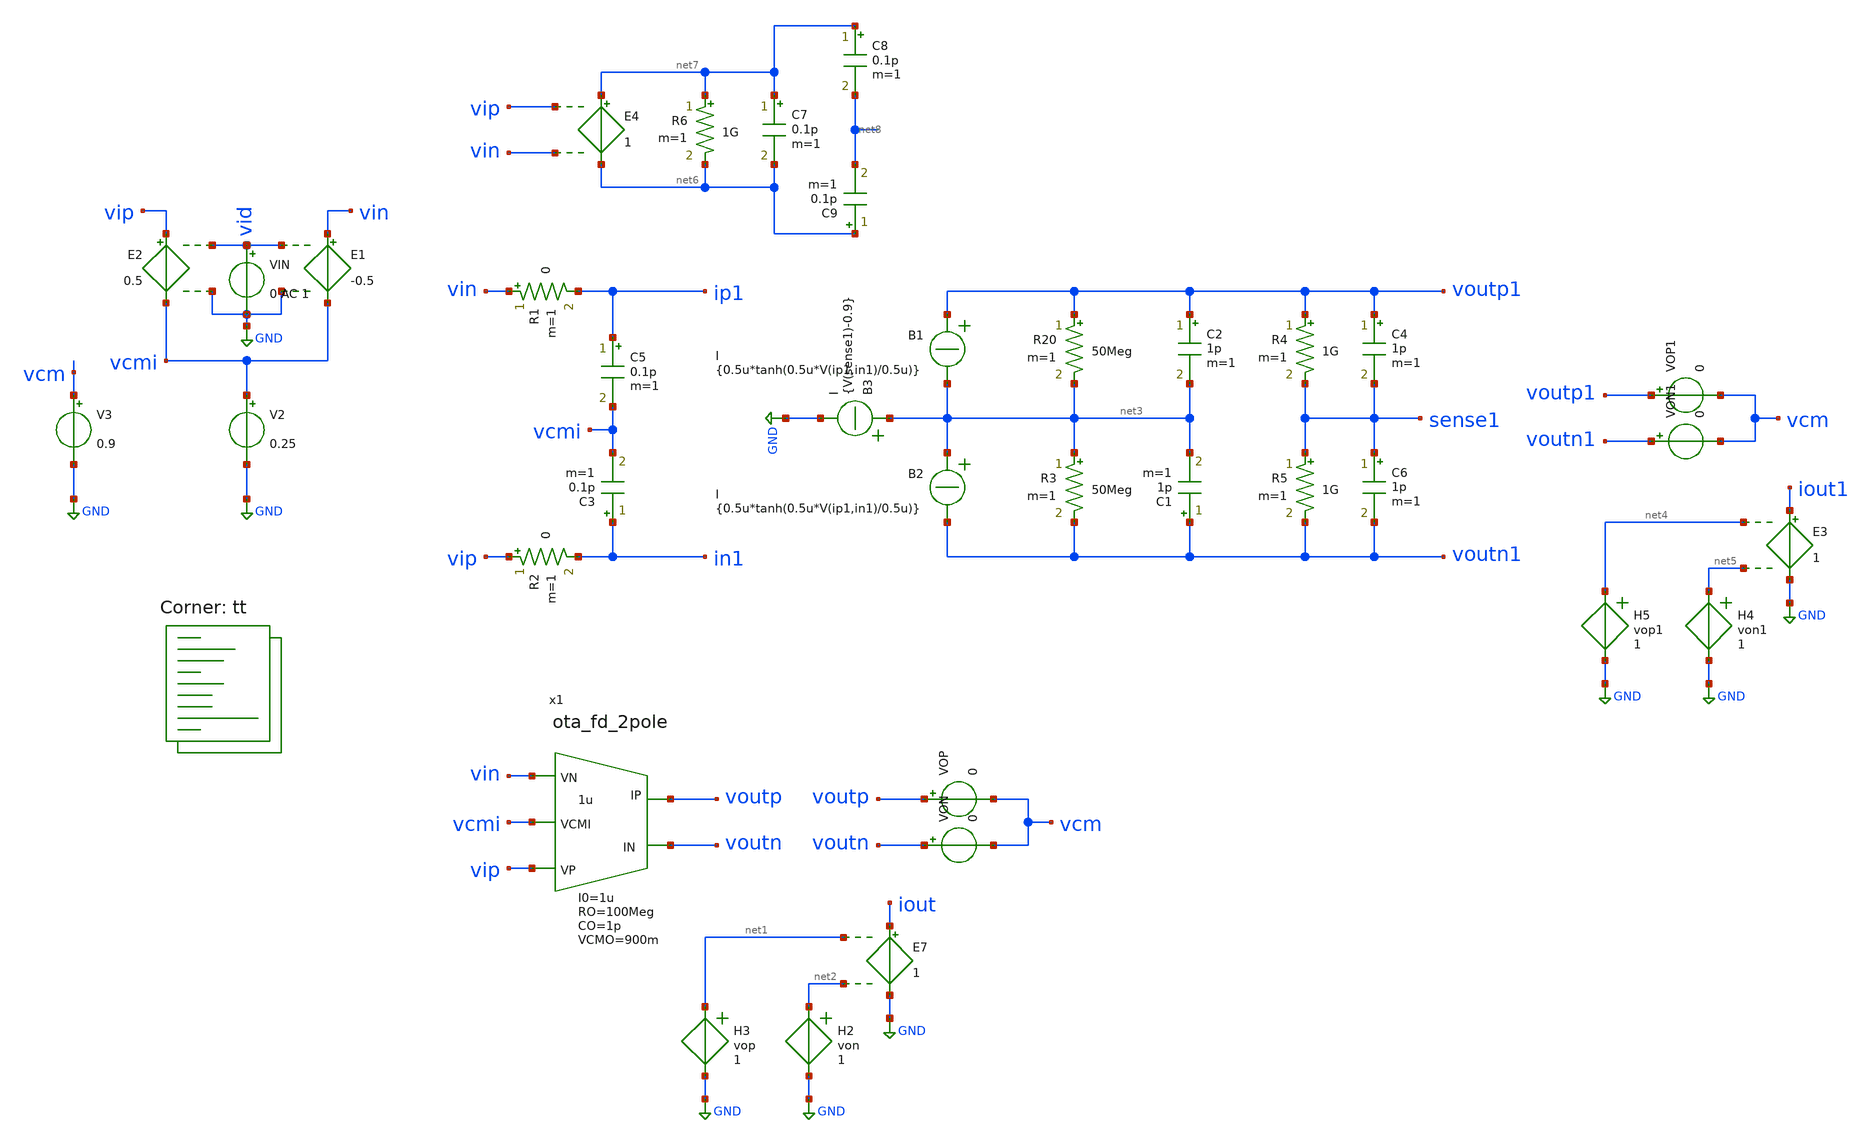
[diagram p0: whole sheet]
** sch_path: circuit-level/xschem/macro-models/ota_macro_fullydiff.sch
**.subckt ota_macro_fullydiff
V2 vcmi GND 0.25
E1 vin vcmi vid GND -0.5
E2 vip vcmi vid GND 0.5
VIN vid GND 0 AC 1
E7 iout GND net1 net2 1
R20 voutp1 net3 50Meg m=1
R3 net3 voutn1 50Meg m=1
C5 ip1 vcmi 0.1p m=1
C3 in1 vcmi 0.1p m=1
V3 vcm GND 0.9
R1 vin ip1 0 m=1
R2 vip in1 0 m=1
C1 voutn1 net3 1p m=1
C2 voutp1 net3 1p m=1
B1 voutp1 net3 I = {0.5u*tanh(0.5u*V(ip1,in1)/0.5u)}
B2 net3 voutn1 I = {0.5u*tanh(0.5u*V(ip1,in1)/0.5u)}
R4 voutp1 sense1 1G m=1
R5 sense1 voutn1 1G m=1
VOP voutp vcm 0
VON voutn vcm 0
H2 net2 GND von 1
H3 net1 GND vop 1
VOP1 voutp1 vcm 0
VON1 voutn1 vcm 0
E3 iout1 GND net4 net5 1
H4 net5 GND von1 1
H5 net4 GND vop1 1
C4 voutp1 sense1 1p m=1
C6 sense1 voutn1 1p m=1
B3 net3 GND I = {V(sense1)-0.9}
x1 vin voutp voutn vip vcmi ota_fd_2pole GM=1u RO=100Meg CO=1p RP=0 CP=0.1p VCMO=900m I0=1u
E4 net7 net6 vip vin 1
C7 net7 net6 0.1p m=1
R6 net7 net6 1G m=1
C8 net7 net8 0.1p m=1
C9 net6 net8 0.1p m=1
**** begin user architecture code
.lib $::SKYWATER_MODELS/sky130.lib.spice tt


.options savecurrents
.control
save all

let f_sig = 18
let tper_sig = 1/f_sig
let tfr_sig = tper_sig/2
*alter @VIN[PULSE]=[ -0.8 0.8 0 $&tfr_sig $&tfr_sig 1u $&tper_sig 0 ]
alter @VIN[SIN] = [ 0 0.1 $&f_sig 0 0 0 ]
alter @VIN[DC] = 0.0

let tstep = 0.01/f_sig
let tstop = 100/f_sig
let tstart = 0

** Main Simulations
let rl = 1Meg
let pltnr = 1
.options scale = 1
while const.pltnr le 1

	dc VIN -0.81 0.81 0.008

	ac dec 1000 0.1 1e9

	tran $&tstep $&tstop $&tstart


	set pltName = ac$&const.pltnr
       	setplot $pltName
	*setplot ac1
	let A_cell = v(iout)/v(vid)
	plot vdb(A_cell) 180/PI*cph(A_cell)
	let A1 = v(iout1)/v(vid)
	plot vdb(A1) 180/PI*cph(A1)

	set pltName = dc$&const.pltnr
       	setplot $pltName
	*setplot dc1
	let vid = v(vid)


	*let iop = v1#branch
	*let ion = v3#branch
	*let iod = iop-ion

	*plot iod ion iop

	setplot tran1
	let vcmo_cell = (voutp+voutn)/2
	let vcmo_1 = (voutp1+voutn1)/2
	let iop_cell = vop#branch
	let ion_cell = von#branch
	let iop_1 = vop1#branch
	let ion_1 = von1#branch
	let io_diff_cell = vop#branch - von#branch
	let io_diff_1 = vop1#branch - von1#branch
	let gm_cell = abs(io_diff_cell+1e-15)/abs(vid+1e-15)
	let gm_1 = abs(io_diff_1+1e-15)/abs(vid+1e-15)
	plot vcmo_cell vcmo_1
	plot io_diff_cell io_diff_1
	plot gm_cell gm_1
	plot v(vid)
	plot iop_cell ion_cell
	plot iop_1 ion_1



       	let const.pltnr = const.pltnr + 1
end
op
remzerovec
write gm_c_ota_int_ideal.raw
.endc

**** end user architecture code
**.ends

* expanding   symbol:  /foss/designs/macro-models/ota_fd_2pole.sym # of pins=5
** sym_path: circuit-level/xschem/macro-models/ota_fd_2pole.sym
** sch_path: circuit-level/xschem/macro-models/ota_fd_2pole.sch
.subckt ota_fd_2pole VN IP IN VP VCMI  GM=1u RO=100Meg CO=1p RP=0 CP=0.1p VCMO=0 I0=1u
*.ipin VP
*.ipin VN
*.opin IP
*.opin IN
*.ipin VCMI
R3 IP net1 {{RO}/2} m=1
R4 IN net1 {{RO}/2} m=1
C3 IP net1 {2*{CO}} m=1
R5 VN ip1 {RP} m=1
C4 ip1 VCMI {CP} m=1
C6 in1 VCMI {CP} m=1
C8 IN net1 {2*{CO}} m=1
R7 VP in1 {RP} m=1
B2 IP net1 I = {{I0}*tanh({GM}/2*V(ip1,in1)/{I0})}
B1 net1 IN I = {{I0}*tanh({GM}/2*V(ip1,in1)/{I0})}
B5 net1 GND I = {{VCMO}-(V(IP)+V(IN))/2}
.ends

.GLOBAL GND
.end
